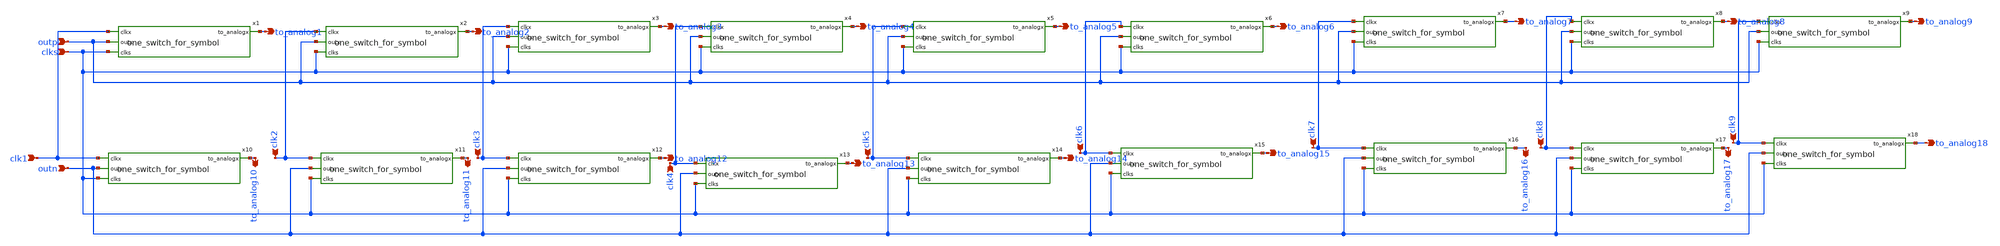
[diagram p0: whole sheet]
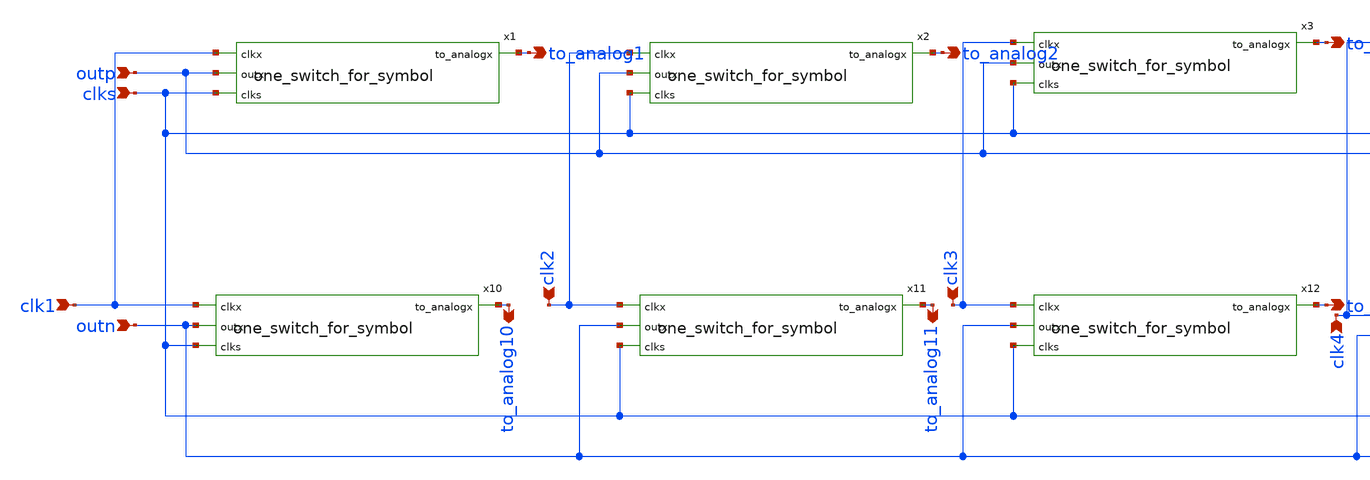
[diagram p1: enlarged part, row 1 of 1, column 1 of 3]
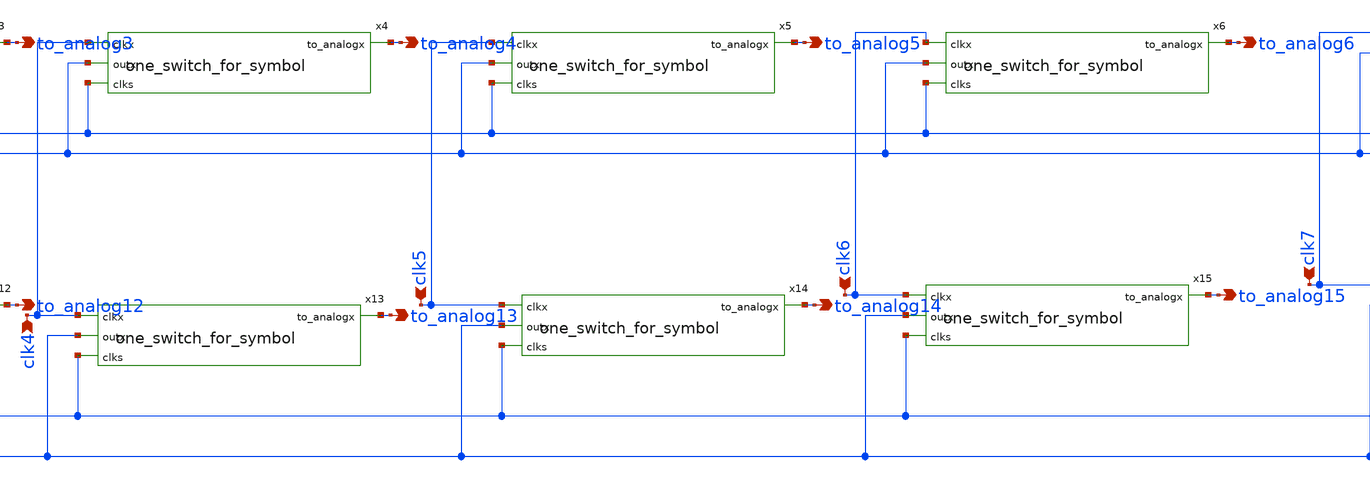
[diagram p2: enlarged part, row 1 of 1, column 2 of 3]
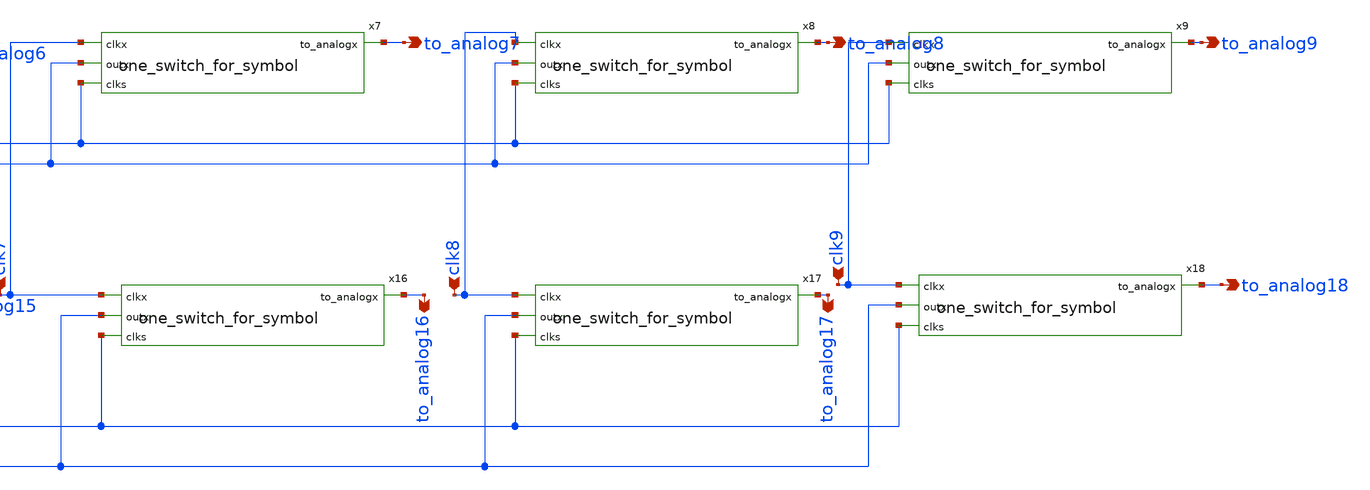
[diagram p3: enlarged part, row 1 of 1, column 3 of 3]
** sch_path: switch_bank.sch
**.subckt switch_bank clk1 outp clks outn clk2 clk3 clk4 clk5 clk6 clk7 clk8 clk9 to_analog1
*+ to_analog2 to_analog3 to_analog4 to_analog5 to_analog6 to_analog7 to_analog8 to_analog9 to_analog18
*+ to_analog17 to_analog16 to_analog15 to_analog14 to_analog13 to_analog12 to_analog11 to_analog10
*.ipin clk1
*.ipin outp
*.ipin clks
*.ipin outn
*.ipin clk2
*.ipin clk3
*.ipin clk4
*.ipin clk5
*.ipin clk6
*.ipin clk7
*.ipin clk8
*.ipin clk9
*.opin to_analog1
*.opin to_analog2
*.opin to_analog3
*.opin to_analog4
*.opin to_analog5
*.opin to_analog6
*.opin to_analog7
*.opin to_analog8
*.opin to_analog9
*.opin to_analog18
*.opin to_analog17
*.opin to_analog16
*.opin to_analog15
*.opin to_analog14
*.opin to_analog13
*.opin to_analog12
*.opin to_analog11
*.opin to_analog10
x1 clk1 to_analog1 outp clks one_switch_for_symbol
x2 clk2 to_analog2 outp clks one_switch_for_symbol
x3 clk3 to_analog3 outp clks one_switch_for_symbol
x4 clk4 to_analog4 outp clks one_switch_for_symbol
x5 clk5 to_analog5 outp clks one_switch_for_symbol
x6 clk6 to_analog6 outp clks one_switch_for_symbol
x7 clk7 to_analog7 outp clks one_switch_for_symbol
x8 clk8 to_analog8 outp clks one_switch_for_symbol
x9 clk9 to_analog9 outp clks one_switch_for_symbol
x10 clk1 to_analog10 outn clks one_switch_for_symbol
x11 clk2 to_analog11 outn clks one_switch_for_symbol
x12 clk3 to_analog12 outn clks one_switch_for_symbol
x13 clk4 to_analog13 outn clks one_switch_for_symbol
x14 clk5 to_analog14 outn clks one_switch_for_symbol
x15 clk6 to_analog15 outn clks one_switch_for_symbol
x16 clk7 to_analog16 outn clks one_switch_for_symbol
x17 clk8 to_analog17 outn clks one_switch_for_symbol
x18 clk9 to_analog18 outn clks one_switch_for_symbol
**.ends

* expanding   symbol:  /home/cegrahul/Desktop/fyp/one_switch_for_symbol.sym # of pins=4
** sym_path: one_switch_for_symbol.sym
** sch_path: one_switch_for_symbol.sch
.subckt one_switch_for_symbol clkx to_analogx outx clks
*.ipin clkx
*.ipin outx
*.ipin clks
*.opin to_analogx
x2 clkx outx clks VGND VNB VPB VPWR net1 net2 sky130_fd_sc_hd__dfrbp_1
x1 clkx net1 VGND VNB VPB VPWR net3 sky130_fd_sc_hd__and2_1
x3 net3 VGND VNB VPB VPWR to_analogx sky130_fd_sc_hd__inv_1
.ends

.end
